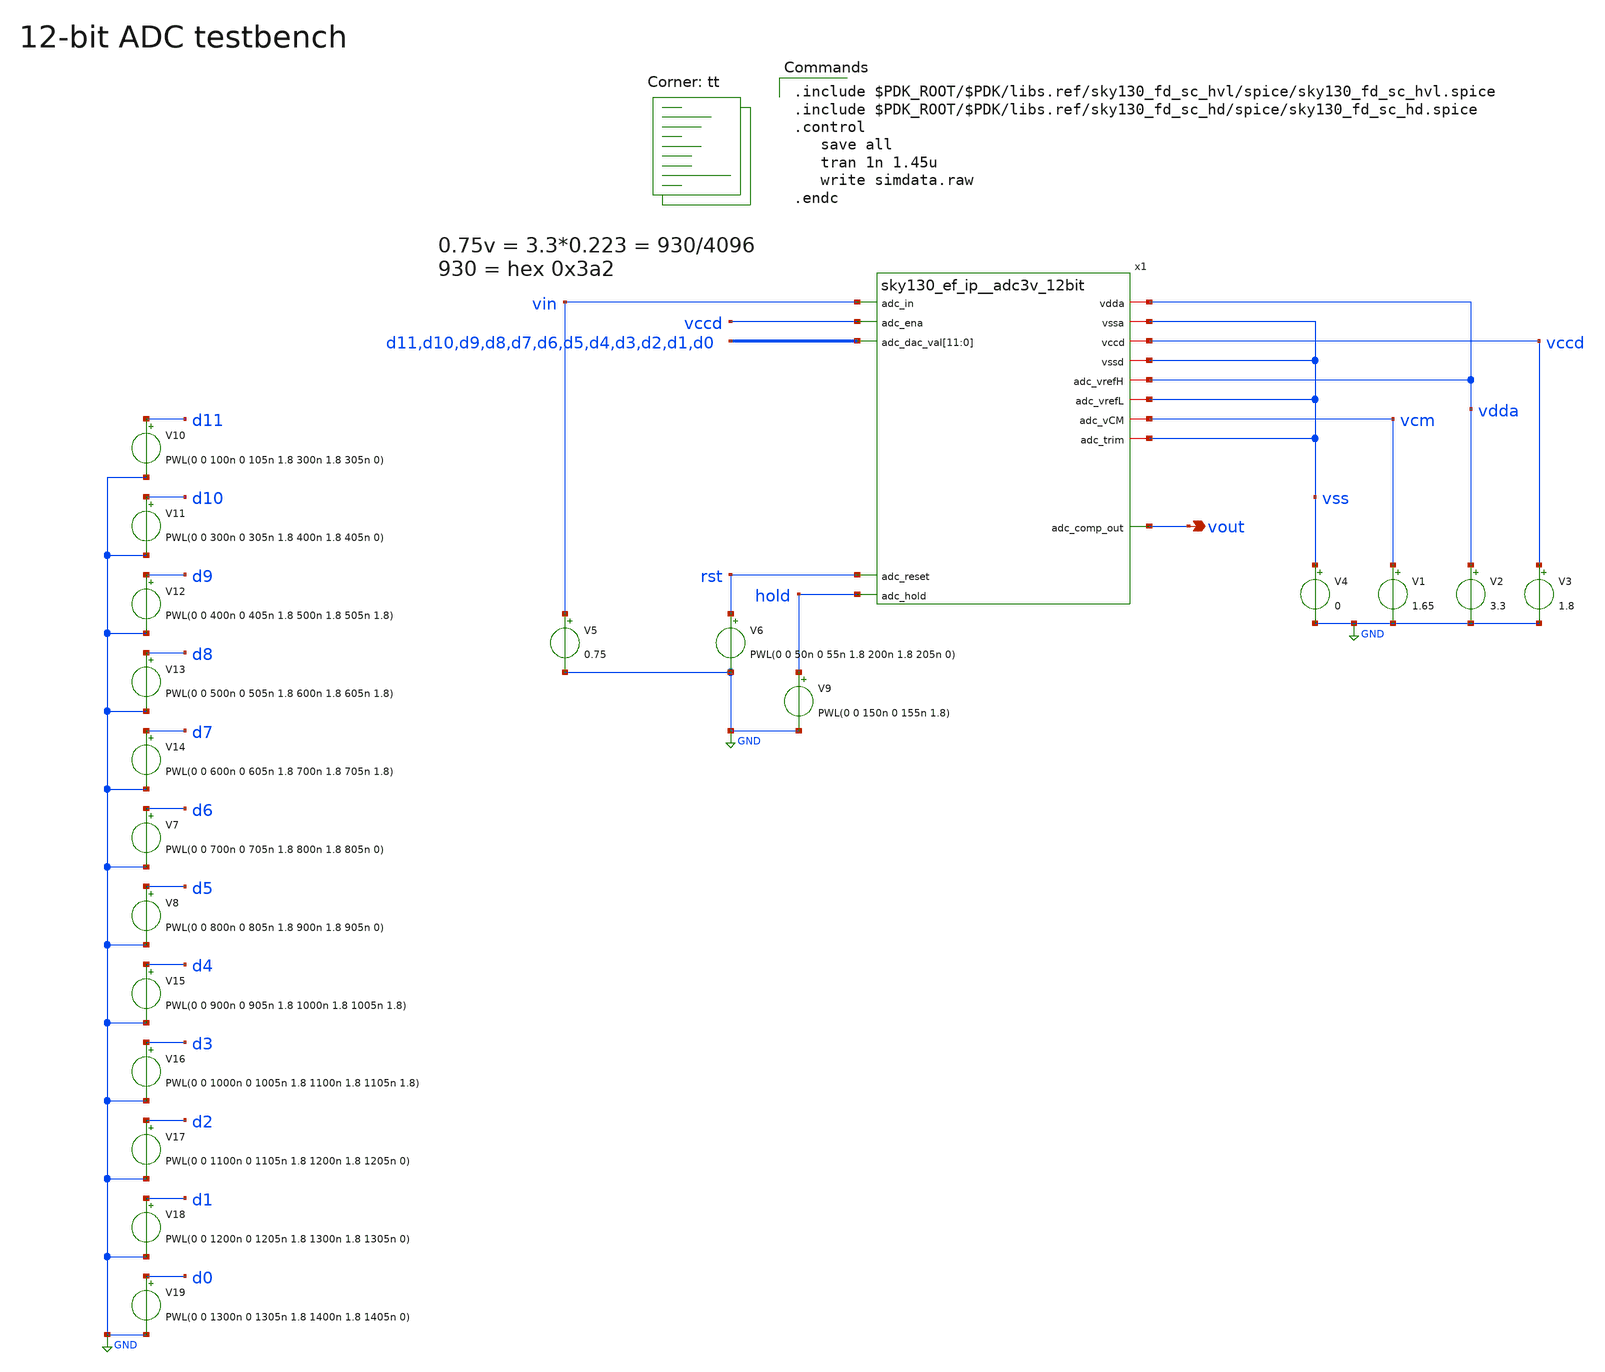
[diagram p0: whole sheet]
** sch_path: ip_references/adc/xschem/adc_tb.sch
**.subckt adc_tb vout
*.opin vout
x1 vdda vss vccd vss vdda vss vin vccd d11 d10 d9 d8 d7 d6 d5 d4 d3 d2 d1 d0 vout rst vcm vss hold
+ sky130_ef_ip__adc3v_12bit
V1 vcm GND 1.65
V2 vdda GND 3.3
V3 vccd GND 1.8
V4 vss GND 0
V5 vin GND 0.75
V6 rst GND PWL(0 0 50n 0 55n 1.8 200n 1.8 205n 0)
V9 hold GND PWL(0 0 150n 0 155n 1.8)
V10 d11 GND PWL(0 0 100n 0 105n 1.8 300n 1.8 305n 0)
V11 d10 GND PWL(0 0 300n 0 305n 1.8 400n 1.8 405n 0)
V12 d9 GND PWL(0 0 400n 0 405n 1.8 500n 1.8 505n 1.8)
V13 d8 GND PWL(0 0 500n 0 505n 1.8 600n 1.8 605n 1.8)
V14 d7 GND PWL(0 0 600n 0 605n 1.8 700n 1.8 705n 1.8)
V7 d6 GND PWL(0 0 700n 0 705n 1.8 800n 1.8 805n 0)
V8 d5 GND PWL(0 0 800n 0 805n 1.8 900n 1.8 905n 0)
V15 d4 GND PWL(0 0 900n 0 905n 1.8 1000n 1.8 1005n 1.8)
V16 d3 GND PWL(0 0 1000n 0 1005n 1.8 1100n 1.8 1105n 1.8)
V17 d2 GND PWL(0 0 1100n 0 1105n 1.8 1200n 1.8 1205n 0)
V18 d1 GND PWL(0 0 1200n 0 1205n 1.8 1300n 1.8 1305n 0)
V19 d0 GND PWL(0 0 1300n 0 1305n 1.8 1400n 1.8 1405n 0)
**** begin user architecture code
.lib $::SKYWATER_MODELS/sky130.lib.spice tt

.include $PDK_ROOT/$PDK/libs.ref/sky130_fd_sc_hvl/spice/sky130_fd_sc_hvl.spice
.include $PDK_ROOT/$PDK/libs.ref/sky130_fd_sc_hd/spice/sky130_fd_sc_hd.spice
.control
   save all
   tran 1n 1.45u
   write simdata.raw
.endc


**** end user architecture code
**.ends
.GLOBAL GND
.end
